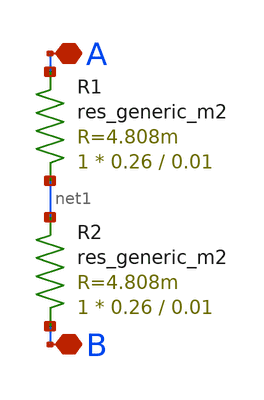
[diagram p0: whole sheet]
** sch_path: common/tk_em2s.sch
* Copyright 2023 David Mitchell Bailey
* Licensed under the Apache License, Version 2.0 (the "License");
* you may not use this file except in compliance with the License.
* You may obtain a copy of the License at
* https://www.apache.org/licenses/LICENSE-2.0
* Unless required by applicable law or agreed to in writing, software
* distributed under the License is distributed on an "AS IS" BASIS,
* WITHOUT WARRANTIES OR CONDITIONS OF ANY KIND, either express or implied.
* See the License for the specific language governing permissions and
* limitations under the License.
**.subckt tk_em2s A B
*.iopin A
*.iopin B
R1 net1 A sky130_fd_pr__res_generic_m2 W=0.26 L=0.01 m=1
R2 B net1 sky130_fd_pr__res_generic_m2 W=0.26 L=0.01 m=1
**.ends
.end
